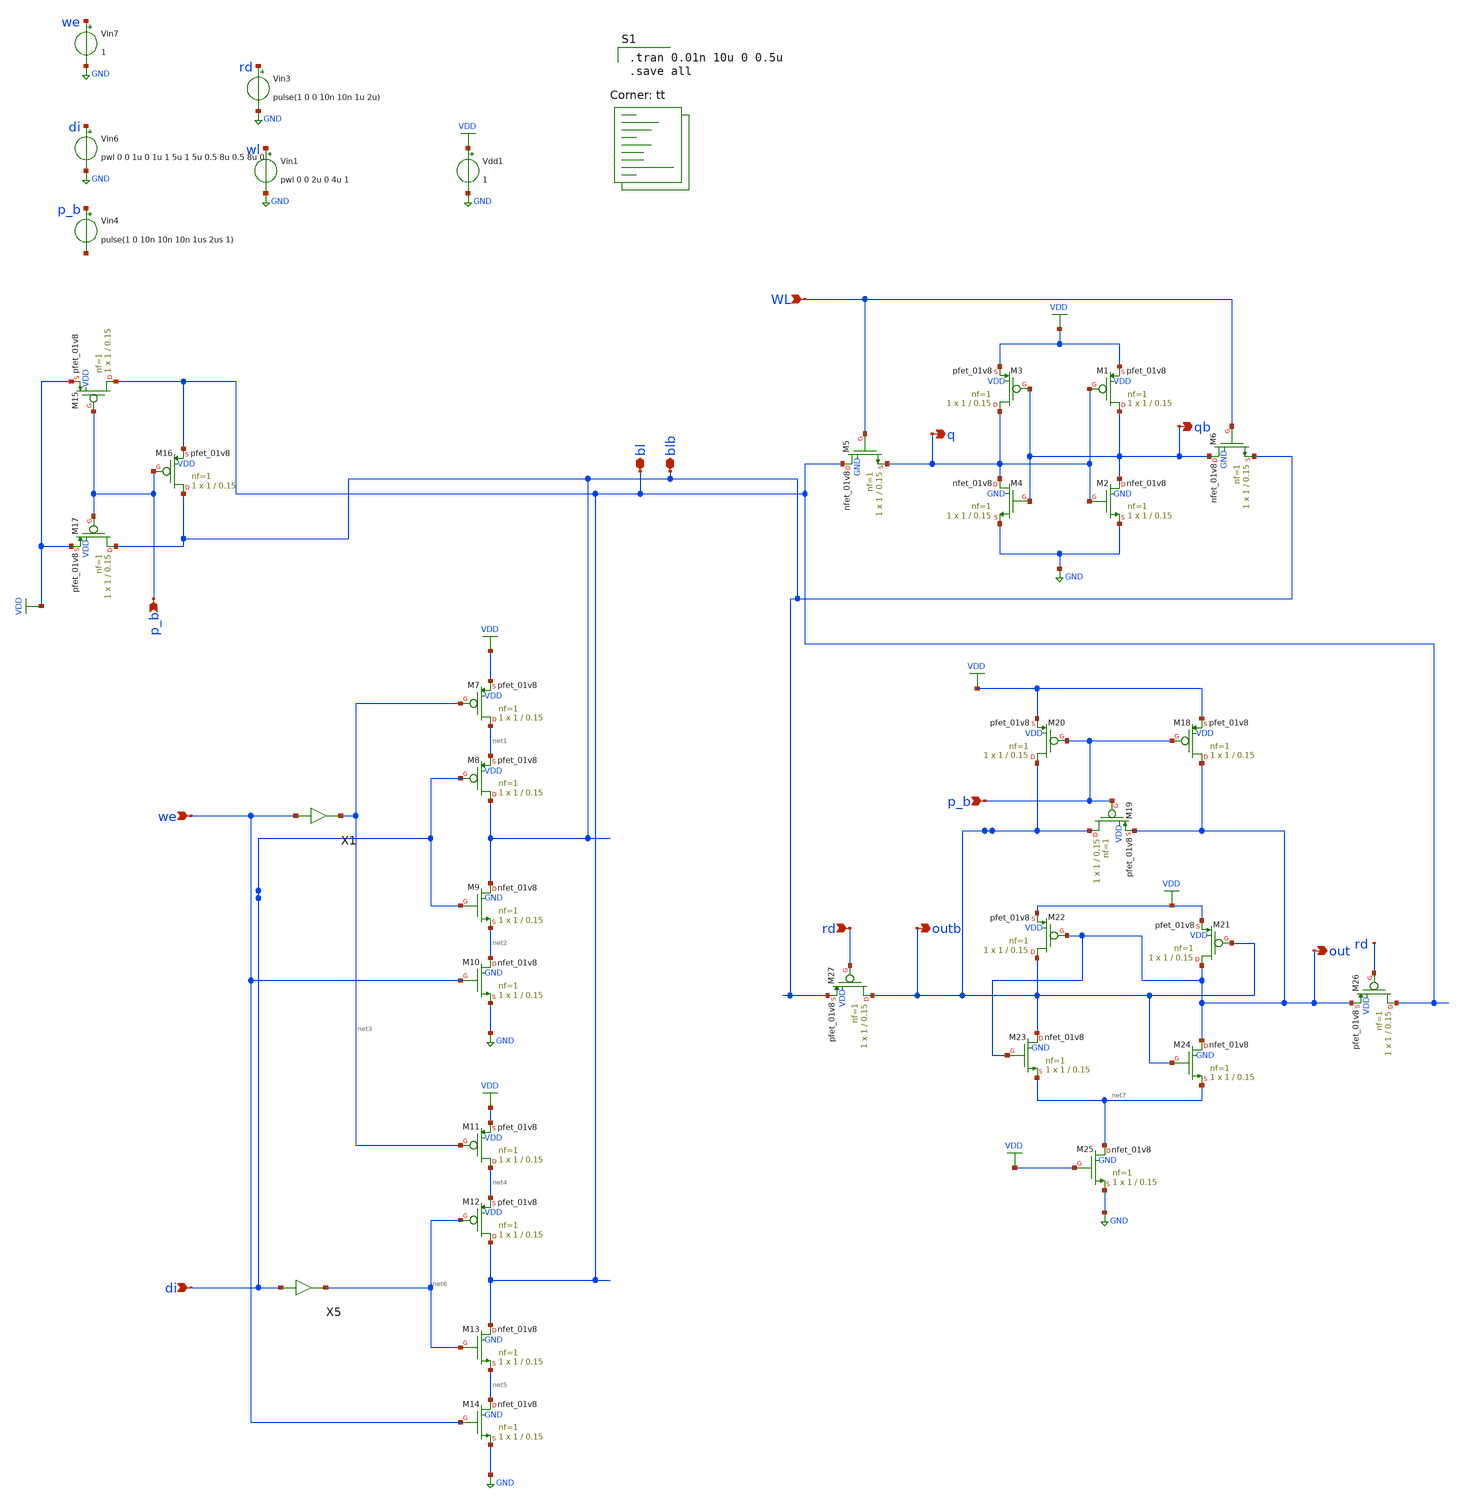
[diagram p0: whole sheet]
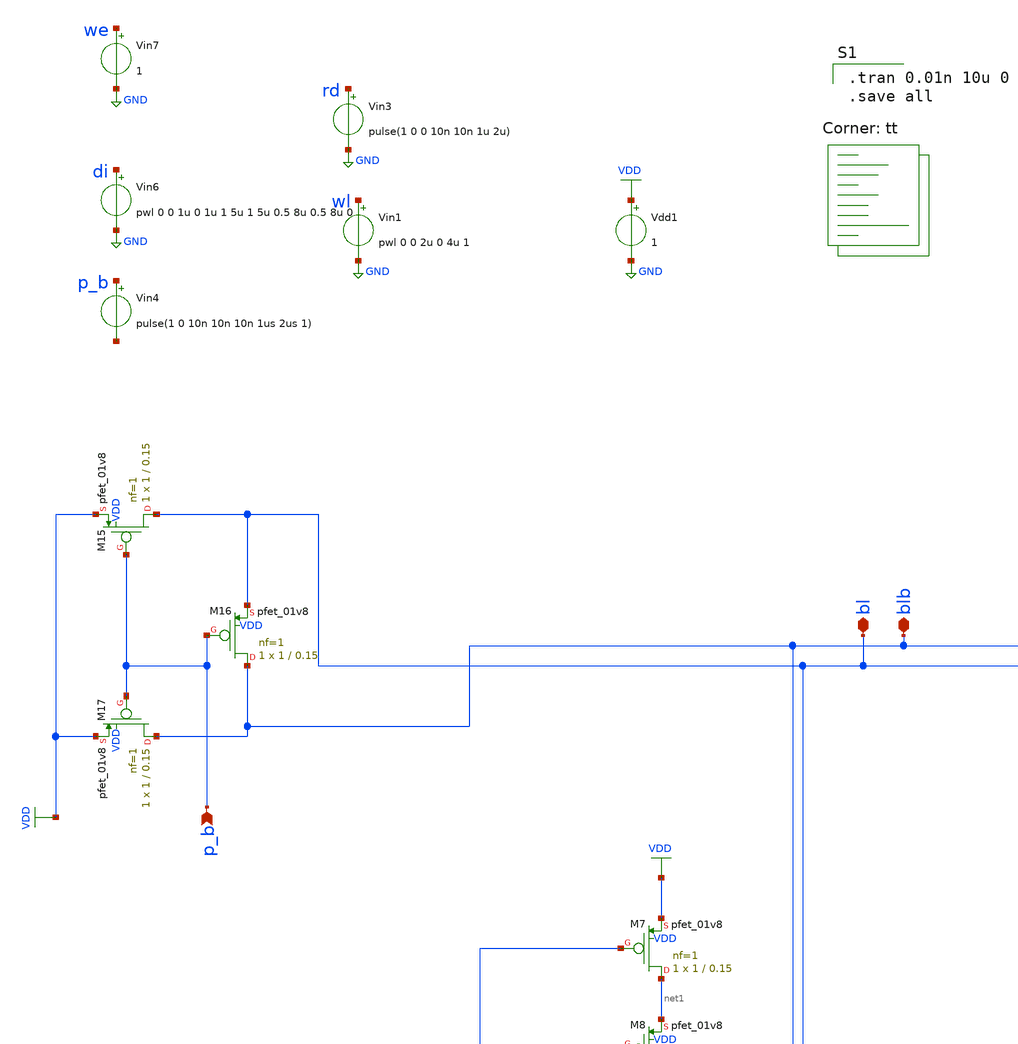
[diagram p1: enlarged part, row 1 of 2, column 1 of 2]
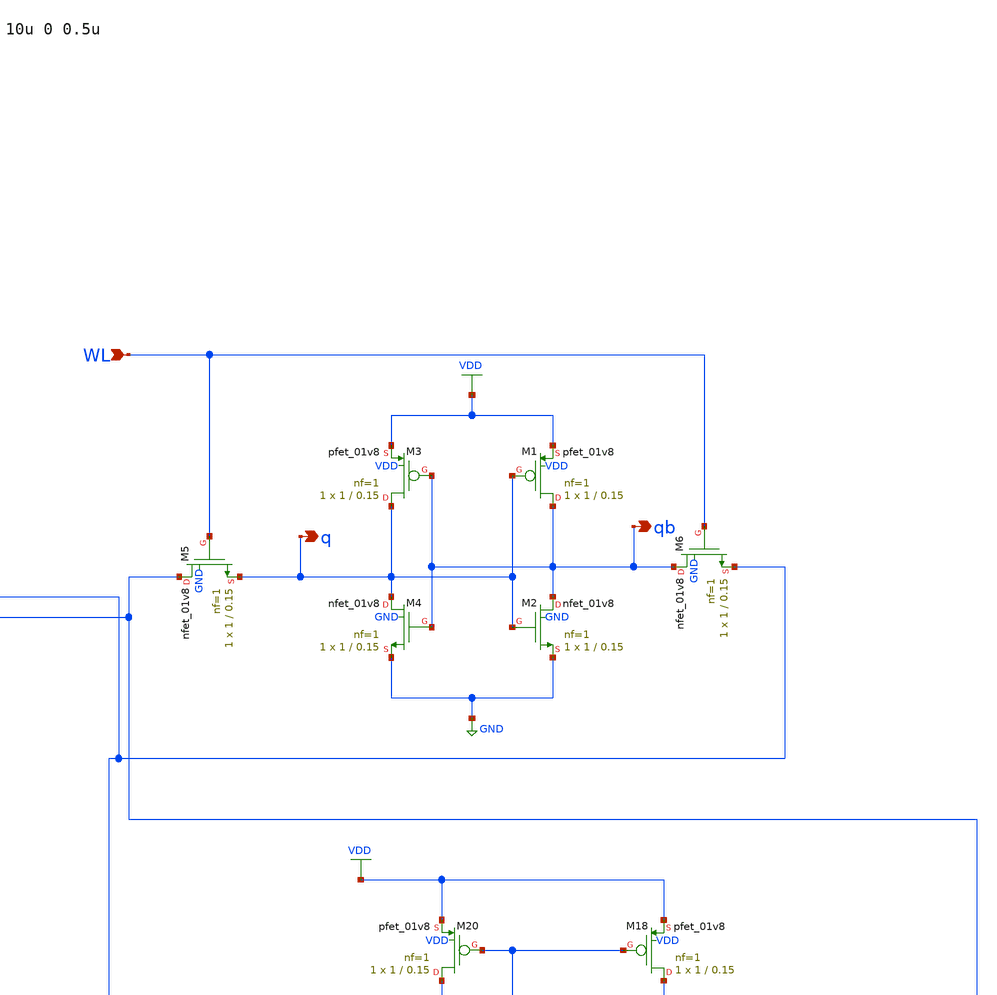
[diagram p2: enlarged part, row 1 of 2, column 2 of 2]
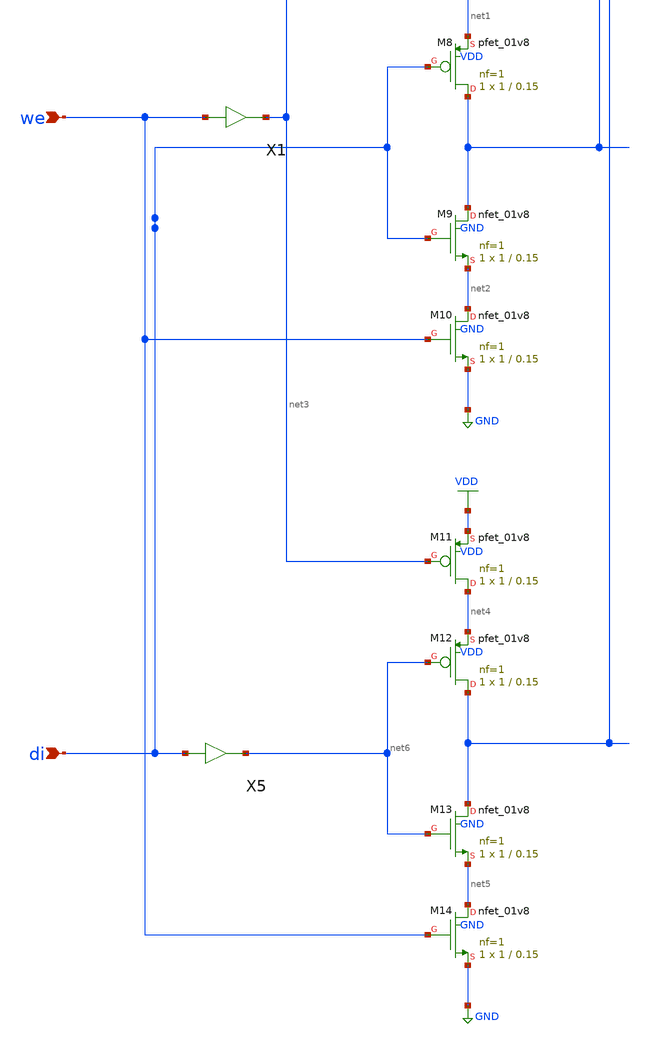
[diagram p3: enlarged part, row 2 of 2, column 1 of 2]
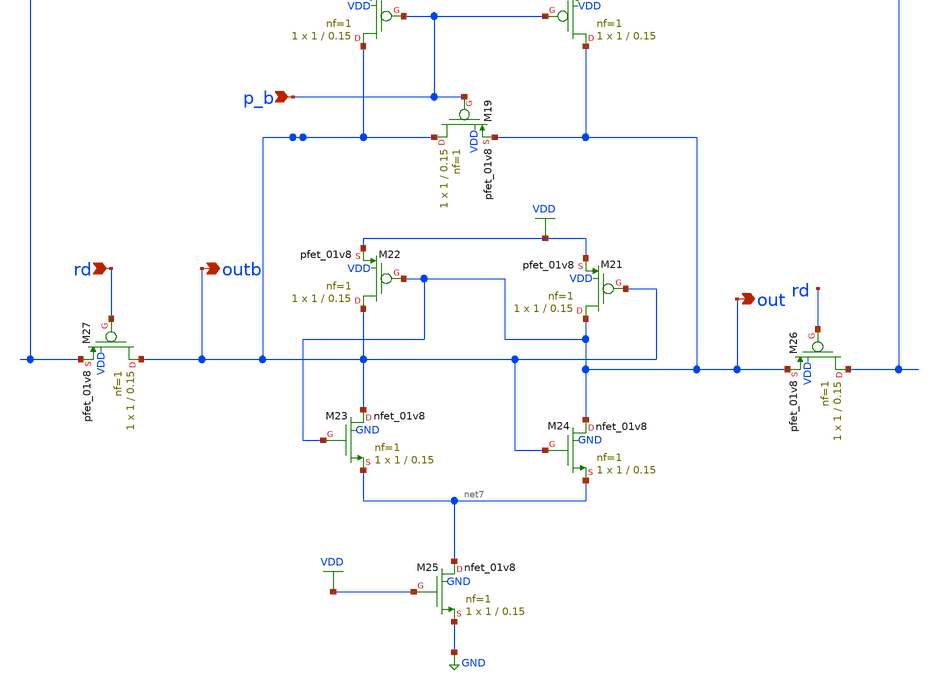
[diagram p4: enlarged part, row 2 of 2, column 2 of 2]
** sch_path: gates/Memory/1x1 bit sramSIM.sch
**.subckt 1x1 bit sramSIM WL qb q we di p_b p_b rd out outb blb bl
*.ipin WL
*.opin qb
*.opin q
*.ipin we
*.ipin di
*.ipin p_b
*.ipin p_b
*.ipin rd
*.opin out
*.opin outb
*.iopin blb
*.iopin bl
Vdd1 VDD GND 1
Vin1 wl GND pwl 0 0 2u 0 4u 1
Vin3 rd GND pulse(1 0 0 10n 10n 1u 2u)
Vin4 p_b net8 pulse(1 0 10n 10n 10n 1us 2us 1)
Vin6 di GND pwl 0 0 1u 0 1u 1 5u 1 5u 0.5 8u 0.5 8u 0
Vin7 we GND 1
XM1 qb q VDD VDD sky130_fd_pr__pfet_01v8 L=0.15 W=1 nf=1 ad='int((nf+1)/2) * W/nf * 0.29' as='int((nf+2)/2) * W/nf * 0.29'
+ pd='2*int((nf+1)/2) * (W/nf + 0.29)' ps='2*int((nf+2)/2) * (W/nf + 0.29)' nrd='0.29 / W' nrs='0.29 / W'
+ sa=0 sb=0 sd=0 mult=1 m=1
XM2 qb q GND GND sky130_fd_pr__nfet_01v8 L=0.15 W=1 nf=1 ad='int((nf+1)/2) * W/nf * 0.29' as='int((nf+2)/2) * W/nf * 0.29'
+ pd='2*int((nf+1)/2) * (W/nf + 0.29)' ps='2*int((nf+2)/2) * (W/nf + 0.29)' nrd='0.29 / W' nrs='0.29 / W'
+ sa=0 sb=0 sd=0 mult=1 m=1
XM3 q qb VDD VDD sky130_fd_pr__pfet_01v8 L=0.15 W=1 nf=1 ad='int((nf+1)/2) * W/nf * 0.29' as='int((nf+2)/2) * W/nf * 0.29'
+ pd='2*int((nf+1)/2) * (W/nf + 0.29)' ps='2*int((nf+2)/2) * (W/nf + 0.29)' nrd='0.29 / W' nrs='0.29 / W'
+ sa=0 sb=0 sd=0 mult=1 m=1
XM4 q qb GND GND sky130_fd_pr__nfet_01v8 L=0.15 W=1 nf=1 ad='int((nf+1)/2) * W/nf * 0.29' as='int((nf+2)/2) * W/nf * 0.29'
+ pd='2*int((nf+1)/2) * (W/nf + 0.29)' ps='2*int((nf+2)/2) * (W/nf + 0.29)' nrd='0.29 / W' nrs='0.29 / W'
+ sa=0 sb=0 sd=0 mult=1 m=1
XM5 bl WL q GND sky130_fd_pr__nfet_01v8 L=0.15 W=1 nf=1 ad='int((nf+1)/2) * W/nf * 0.29' as='int((nf+2)/2) * W/nf * 0.29'
+ pd='2*int((nf+1)/2) * (W/nf + 0.29)' ps='2*int((nf+2)/2) * (W/nf + 0.29)' nrd='0.29 / W' nrs='0.29 / W'
+ sa=0 sb=0 sd=0 mult=1 m=1
XM6 qb WL blb GND sky130_fd_pr__nfet_01v8 L=0.15 W=1 nf=1 ad='int((nf+1)/2) * W/nf * 0.29' as='int((nf+2)/2) * W/nf * 0.29'
+ pd='2*int((nf+1)/2) * (W/nf + 0.29)' ps='2*int((nf+2)/2) * (W/nf + 0.29)' nrd='0.29 / W' nrs='0.29 / W'
+ sa=0 sb=0 sd=0 mult=1 m=1
X1 we net3 inv_vtc
X5 di net6 inv_vtc
XM7 net1 net3 VDD VDD sky130_fd_pr__pfet_01v8 L=0.15 W=1 nf=1 ad='int((nf+1)/2) * W/nf * 0.29' as='int((nf+2)/2) * W/nf * 0.29'
+ pd='2*int((nf+1)/2) * (W/nf + 0.29)' ps='2*int((nf+2)/2) * (W/nf + 0.29)' nrd='0.29 / W' nrs='0.29 / W'
+ sa=0 sb=0 sd=0 mult=1 m=1
XM8 blb di net1 VDD sky130_fd_pr__pfet_01v8 L=0.15 W=1 nf=1 ad='int((nf+1)/2) * W/nf * 0.29' as='int((nf+2)/2) * W/nf * 0.29'
+ pd='2*int((nf+1)/2) * (W/nf + 0.29)' ps='2*int((nf+2)/2) * (W/nf + 0.29)' nrd='0.29 / W' nrs='0.29 / W'
+ sa=0 sb=0 sd=0 mult=1 m=1
XM9 blb di net2 GND sky130_fd_pr__nfet_01v8 L=0.15 W=1 nf=1 ad='int((nf+1)/2) * W/nf * 0.29' as='int((nf+2)/2) * W/nf * 0.29'
+ pd='2*int((nf+1)/2) * (W/nf + 0.29)' ps='2*int((nf+2)/2) * (W/nf + 0.29)' nrd='0.29 / W' nrs='0.29 / W'
+ sa=0 sb=0 sd=0 mult=1 m=1
XM10 net2 we GND GND sky130_fd_pr__nfet_01v8 L=0.15 W=1 nf=1 ad='int((nf+1)/2) * W/nf * 0.29' as='int((nf+2)/2) * W/nf * 0.29'
+ pd='2*int((nf+1)/2) * (W/nf + 0.29)' ps='2*int((nf+2)/2) * (W/nf + 0.29)' nrd='0.29 / W' nrs='0.29 / W'
+ sa=0 sb=0 sd=0 mult=1 m=1
XM11 net4 net3 VDD VDD sky130_fd_pr__pfet_01v8 L=0.15 W=1 nf=1 ad='int((nf+1)/2) * W/nf * 0.29' as='int((nf+2)/2) * W/nf * 0.29'
+ pd='2*int((nf+1)/2) * (W/nf + 0.29)' ps='2*int((nf+2)/2) * (W/nf + 0.29)' nrd='0.29 / W' nrs='0.29 / W'
+ sa=0 sb=0 sd=0 mult=1 m=1
XM12 bl net6 net4 VDD sky130_fd_pr__pfet_01v8 L=0.15 W=1 nf=1 ad='int((nf+1)/2) * W/nf * 0.29' as='int((nf+2)/2) * W/nf * 0.29'
+ pd='2*int((nf+1)/2) * (W/nf + 0.29)' ps='2*int((nf+2)/2) * (W/nf + 0.29)' nrd='0.29 / W' nrs='0.29 / W'
+ sa=0 sb=0 sd=0 mult=1 m=1
XM13 bl net6 net5 GND sky130_fd_pr__nfet_01v8 L=0.15 W=1 nf=1 ad='int((nf+1)/2) * W/nf * 0.29' as='int((nf+2)/2) * W/nf * 0.29'
+ pd='2*int((nf+1)/2) * (W/nf + 0.29)' ps='2*int((nf+2)/2) * (W/nf + 0.29)' nrd='0.29 / W' nrs='0.29 / W'
+ sa=0 sb=0 sd=0 mult=1 m=1
XM14 net5 we GND GND sky130_fd_pr__nfet_01v8 L=0.15 W=1 nf=1 ad='int((nf+1)/2) * W/nf * 0.29' as='int((nf+2)/2) * W/nf * 0.29'
+ pd='2*int((nf+1)/2) * (W/nf + 0.29)' ps='2*int((nf+2)/2) * (W/nf + 0.29)' nrd='0.29 / W' nrs='0.29 / W'
+ sa=0 sb=0 sd=0 mult=1 m=1
XM15 bl p_b VDD VDD sky130_fd_pr__pfet_01v8 L=0.15 W=1 nf=1 ad='int((nf+1)/2) * W/nf * 0.29' as='int((nf+2)/2) * W/nf * 0.29'
+ pd='2*int((nf+1)/2) * (W/nf + 0.29)' ps='2*int((nf+2)/2) * (W/nf + 0.29)' nrd='0.29 / W' nrs='0.29 / W'
+ sa=0 sb=0 sd=0 mult=1 m=1
XM16 blb p_b bl VDD sky130_fd_pr__pfet_01v8 L=0.15 W=1 nf=1 ad='int((nf+1)/2) * W/nf * 0.29' as='int((nf+2)/2) * W/nf * 0.29'
+ pd='2*int((nf+1)/2) * (W/nf + 0.29)' ps='2*int((nf+2)/2) * (W/nf + 0.29)' nrd='0.29 / W' nrs='0.29 / W'
+ sa=0 sb=0 sd=0 mult=1 m=1
XM17 blb p_b VDD VDD sky130_fd_pr__pfet_01v8 L=0.15 W=1 nf=1 ad='int((nf+1)/2) * W/nf * 0.29' as='int((nf+2)/2) * W/nf * 0.29'
+ pd='2*int((nf+1)/2) * (W/nf + 0.29)' ps='2*int((nf+2)/2) * (W/nf + 0.29)' nrd='0.29 / W' nrs='0.29 / W'
+ sa=0 sb=0 sd=0 mult=1 m=1
XM18 out p_b VDD VDD sky130_fd_pr__pfet_01v8 L=0.15 W=1 nf=1 ad='int((nf+1)/2) * W/nf * 0.29' as='int((nf+2)/2) * W/nf * 0.29'
+ pd='2*int((nf+1)/2) * (W/nf + 0.29)' ps='2*int((nf+2)/2) * (W/nf + 0.29)' nrd='0.29 / W' nrs='0.29 / W'
+ sa=0 sb=0 sd=0 mult=1 m=1
XM19 outb p_b out VDD sky130_fd_pr__pfet_01v8 L=0.15 W=1 nf=1 ad='int((nf+1)/2) * W/nf * 0.29' as='int((nf+2)/2) * W/nf * 0.29'
+ pd='2*int((nf+1)/2) * (W/nf + 0.29)' ps='2*int((nf+2)/2) * (W/nf + 0.29)' nrd='0.29 / W' nrs='0.29 / W'
+ sa=0 sb=0 sd=0 mult=1 m=1
XM20 outb p_b VDD VDD sky130_fd_pr__pfet_01v8 L=0.15 W=1 nf=1 ad='int((nf+1)/2) * W/nf * 0.29' as='int((nf+2)/2) * W/nf * 0.29'
+ pd='2*int((nf+1)/2) * (W/nf + 0.29)' ps='2*int((nf+2)/2) * (W/nf + 0.29)' nrd='0.29 / W' nrs='0.29 / W'
+ sa=0 sb=0 sd=0 mult=1 m=1
XM21 out outb VDD VDD sky130_fd_pr__pfet_01v8 L=0.15 W=1 nf=1 ad='int((nf+1)/2) * W/nf * 0.29' as='int((nf+2)/2) * W/nf * 0.29'
+ pd='2*int((nf+1)/2) * (W/nf + 0.29)' ps='2*int((nf+2)/2) * (W/nf + 0.29)' nrd='0.29 / W' nrs='0.29 / W'
+ sa=0 sb=0 sd=0 mult=1 m=1
XM22 outb out VDD VDD sky130_fd_pr__pfet_01v8 L=0.15 W=1 nf=1 ad='int((nf+1)/2) * W/nf * 0.29' as='int((nf+2)/2) * W/nf * 0.29'
+ pd='2*int((nf+1)/2) * (W/nf + 0.29)' ps='2*int((nf+2)/2) * (W/nf + 0.29)' nrd='0.29 / W' nrs='0.29 / W'
+ sa=0 sb=0 sd=0 mult=1 m=1
XM23 outb out net7 GND sky130_fd_pr__nfet_01v8 L=0.15 W=1 nf=1 ad='int((nf+1)/2) * W/nf * 0.29' as='int((nf+2)/2) * W/nf * 0.29'
+ pd='2*int((nf+1)/2) * (W/nf + 0.29)' ps='2*int((nf+2)/2) * (W/nf + 0.29)' nrd='0.29 / W' nrs='0.29 / W'
+ sa=0 sb=0 sd=0 mult=1 m=1
XM24 out outb net7 GND sky130_fd_pr__nfet_01v8 L=0.15 W=1 nf=1 ad='int((nf+1)/2) * W/nf * 0.29' as='int((nf+2)/2) * W/nf * 0.29'
+ pd='2*int((nf+1)/2) * (W/nf + 0.29)' ps='2*int((nf+2)/2) * (W/nf + 0.29)' nrd='0.29 / W' nrs='0.29 / W'
+ sa=0 sb=0 sd=0 mult=1 m=1
XM25 net7 VDD GND GND sky130_fd_pr__nfet_01v8 L=0.15 W=1 nf=1 ad='int((nf+1)/2) * W/nf * 0.29' as='int((nf+2)/2) * W/nf * 0.29'
+ pd='2*int((nf+1)/2) * (W/nf + 0.29)' ps='2*int((nf+2)/2) * (W/nf + 0.29)' nrd='0.29 / W' nrs='0.29 / W'
+ sa=0 sb=0 sd=0 mult=1 m=1
XM26 bl rd out VDD sky130_fd_pr__pfet_01v8 L=0.15 W=1 nf=1 ad='int((nf+1)/2) * W/nf * 0.29' as='int((nf+2)/2) * W/nf * 0.29'
+ pd='2*int((nf+1)/2) * (W/nf + 0.29)' ps='2*int((nf+2)/2) * (W/nf + 0.29)' nrd='0.29 / W' nrs='0.29 / W'
+ sa=0 sb=0 sd=0 mult=1 m=1
XM27 outb rd blb VDD sky130_fd_pr__pfet_01v8 L=0.15 W=1 nf=1 ad='int((nf+1)/2) * W/nf * 0.29' as='int((nf+2)/2) * W/nf * 0.29'
+ pd='2*int((nf+1)/2) * (W/nf + 0.29)' ps='2*int((nf+2)/2) * (W/nf + 0.29)' nrd='0.29 / W' nrs='0.29 / W'
+ sa=0 sb=0 sd=0 mult=1 m=1
**** begin user architecture code

.tran 0.01n 10u 0 0.5u
.save all

.lib $::SKYWATER_MODELS/sky130.lib.spice tt
**** end user architecture code
**.ends

* expanding   symbol:  /home/apn/test_xschem_sky130/inv_vtc.sym # of pins=2
** sym_path: gates/Memory/inv_vtc.sym
** sch_path: gates/Memory/inv_vtc.sch
.subckt inv_vtc A Y
*.ipin A
*.opin Y
XM1 Y A VDD VDD sky130_fd_pr__pfet_01v8 L=0.15 W=2 nf=1 ad='int((nf+1)/2) * W/nf * 0.29' as='int((nf+2)/2) * W/nf * 0.29'
+ pd='2*int((nf+1)/2) * (W/nf + 0.29)' ps='2*int((nf+2)/2) * (W/nf + 0.29)' nrd='0.29 / W' nrs='0.29 / W'
+ sa=0 sb=0 sd=0 mult=1 m=1
XM2 Y A GND GND sky130_fd_pr__nfet_01v8 L=0.15 W=1 nf=1 ad='int((nf+1)/2) * W/nf * 0.29' as='int((nf+2)/2) * W/nf * 0.29'
+ pd='2*int((nf+1)/2) * (W/nf + 0.29)' ps='2*int((nf+2)/2) * (W/nf + 0.29)' nrd='0.29 / W' nrs='0.29 / W'
+ sa=0 sb=0 sd=0 mult=1 m=1
.ends

.GLOBAL VDD
.GLOBAL GND
.end
